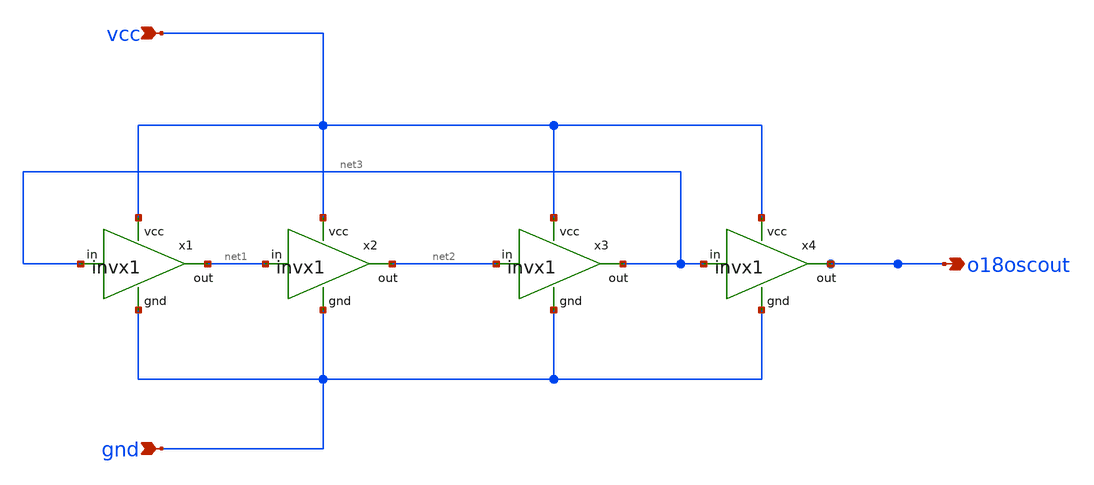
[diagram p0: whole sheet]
** sch_path: xschem/osu_soc_tsmc018/ringosc/ringosc.sch
**.subckt ringosc o18oscout vcc gnd
*.opin o18oscout
*.ipin vcc
*.ipin gnd
x4 vcc net3 o18oscout gnd invx1
x2 vcc net1 net2 gnd invx1
x3 vcc net2 net3 gnd invx1
x1 vcc net3 net1 gnd invx1
**.ends

* expanding   symbol:  ../inverter/invx1.sym # of pins=4
** sym_path: xschem/osu_soc_tsmc018/inverter/invx1.sym
** sch_path: xschem/osu_soc_tsmc018/inverter/invx1.sch
.subckt invx1 vcc in out gnd
*.ipin in
*.opin out
*.ipin vcc
*.ipin gnd
M1 out in vcc vcc pmos w=5u l=0.18u m=1
M2 out in gnd gnd nmos w=5u l=0.18u m=1
.ends

.end
